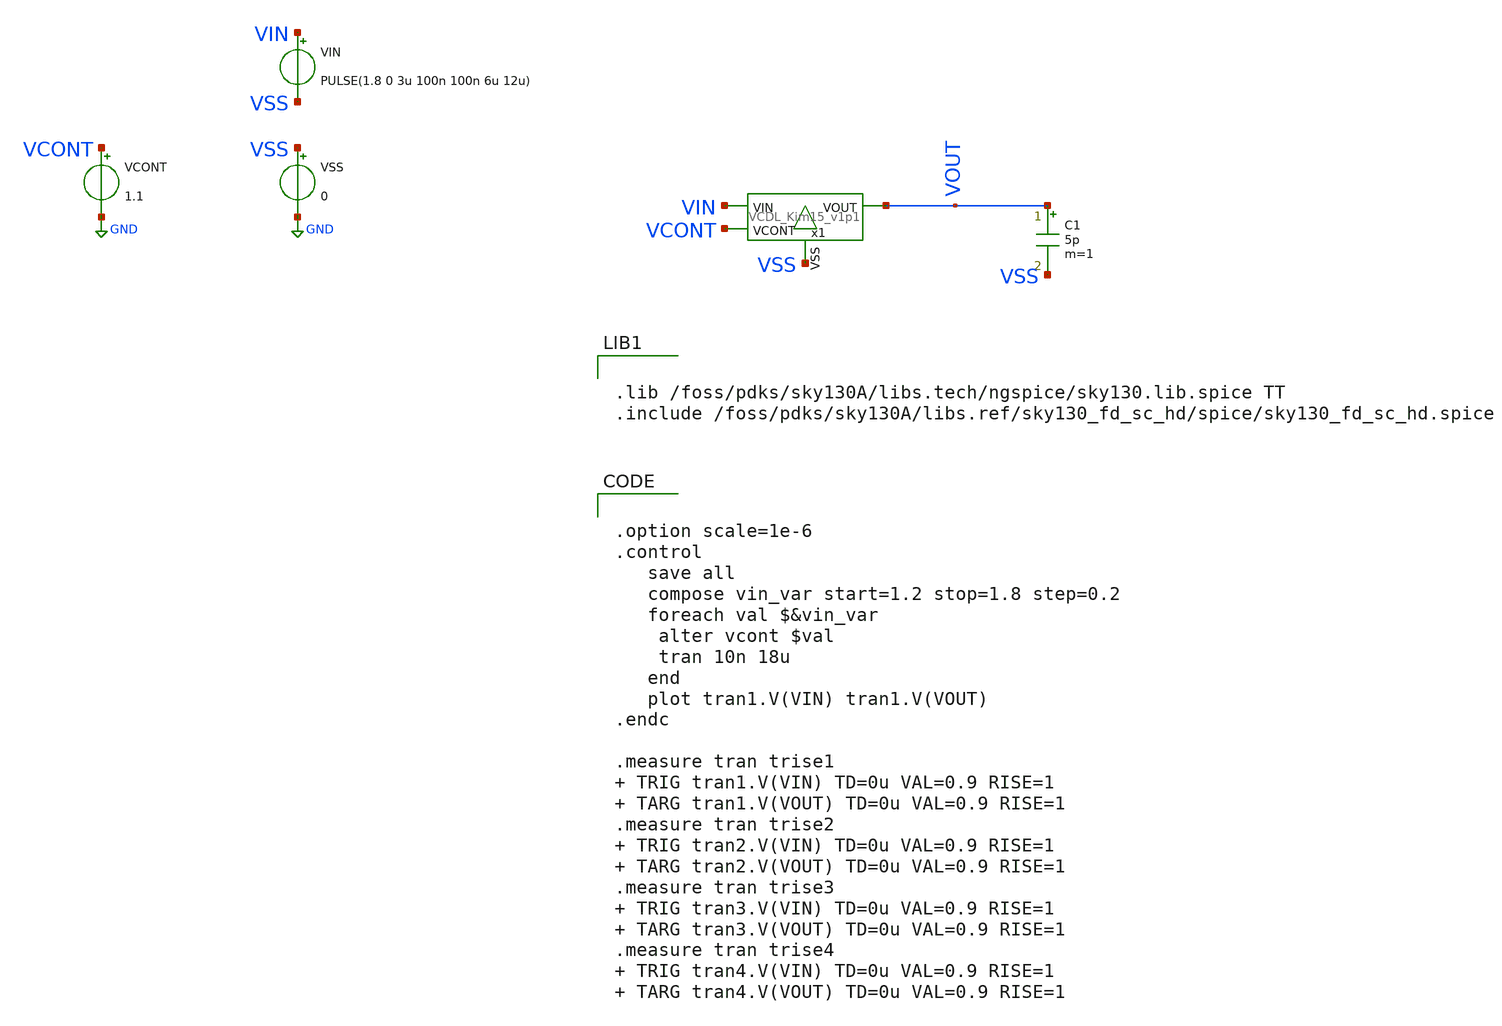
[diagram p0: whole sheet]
** sch_path: xschem/tb_VCDL_Kim15_v1p1.sch
**.subckt tb_VCDL_Kim15_v1p1
VSS VSS GND 0
VIN VIN VSS PULSE(1.8 0 3u 100n 100n 6u 12u)
VCONT VCONT GND 1.1
C1 VOUT VSS 5p m=1
x1 VCONT VOUT VIN VSS VCDL_Kim15_v1p1
**** begin user architecture code


.lib /foss/pdks/sky130A/libs.tech/ngspice/sky130.lib.spice TT
.include /foss/pdks/sky130A/libs.ref/sky130_fd_sc_hd/spice/sky130_fd_sc_hd.spice




.option scale=1e-6
.control
   save all
   compose vin_var start=1.2 stop=1.8 step=0.2
   foreach val $&vin_var
	alter vcont $val
	tran 10n 18u
   end
   plot tran1.V(VIN) tran1.V(VOUT)
.endc

.measure tran trise1   TRIG tran1.V(VIN) TD=0u VAL=0.9 RISE=1  TARG tran1.V(VOUT) TD=0u VAL=0.9
+ RISE=1
.measure tran trise2  TRIG tran2.V(VIN) TD=0u VAL=0.9 RISE=1  TARG tran2.V(VOUT) TD=0u VAL=0.9
+ RISE=1
.measure tran trise3  TRIG tran3.V(VIN) TD=0u VAL=0.9 RISE=1  TARG tran3.V(VOUT) TD=0u VAL=0.9
+ RISE=1
.measure tran trise4  TRIG tran4.V(VIN) TD=0u VAL=0.9 RISE=1  TARG tran4.V(VOUT) TD=0u VAL=0.9
+ RISE=1


**** end user architecture code
**.ends
.GLOBAL GND
.end
